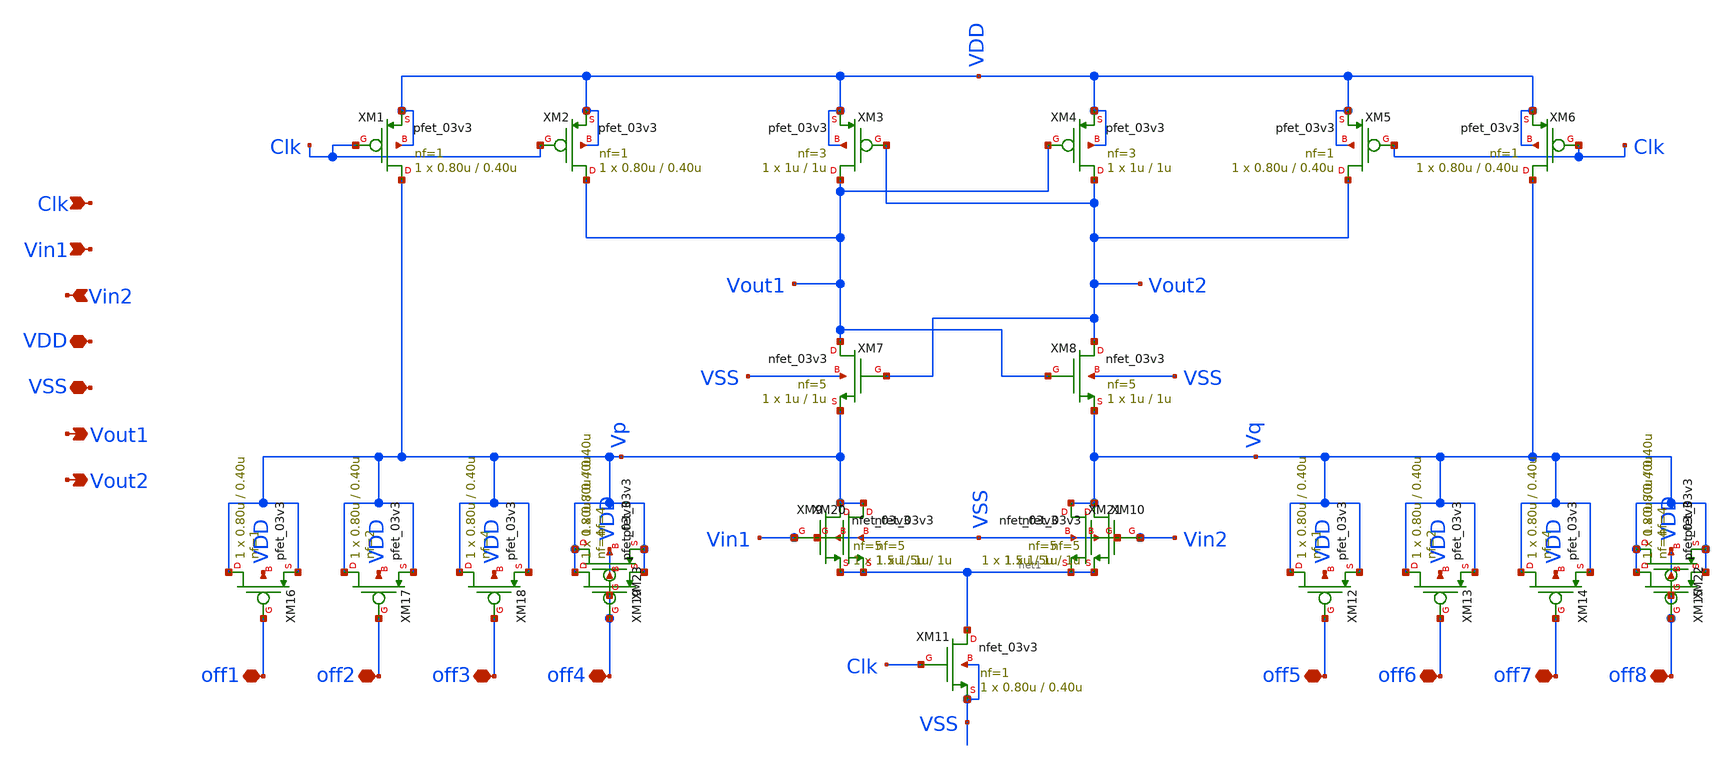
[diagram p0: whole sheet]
** sch_path: designs/comparator/final_magic/lvsclean_SAlatch.sch
**.subckt lvsclean_SAlatch Clk Vin1 Vin2 VDD VSS Vout1 Vout2 off5 off6 off7 off8 off1 off2 off3 off4
*.ipin Clk
*.ipin Vin1
*.ipin Vin2
*.iopin VDD
*.iopin VSS
*.opin Vout1
*.opin Vout2
*.iopin off5
*.iopin off6
*.iopin off7
*.iopin off8
*.iopin off1
*.iopin off2
*.iopin off3
*.iopin off4
XM1 Vp Clk VDD VDD pfet_03v3 L=0.40u W=0.80u nf=1 ad='int((nf+1)/2) * W/nf * 0.18u' as='int((nf+2)/2) * W/nf * 0.18u'
+ pd='2*int((nf+1)/2) * (W/nf + 0.18u)' ps='2*int((nf+2)/2) * (W/nf + 0.18u)' nrd='0.18u / W' nrs='0.18u / W'
+ sa=0 sb=0 sd=0 m=1
XM2 Vout1 Clk VDD VDD pfet_03v3 L=0.40u W=0.80u nf=1 ad='int((nf+1)/2) * W/nf * 0.18u' as='int((nf+2)/2) * W/nf * 0.18u'
+ pd='2*int((nf+1)/2) * (W/nf + 0.18u)' ps='2*int((nf+2)/2) * (W/nf + 0.18u)' nrd='0.18u / W' nrs='0.18u / W'
+ sa=0 sb=0 sd=0 m=1
XM3 Vout1 Vout2 VDD VDD pfet_03v3 L=1u W=1u nf=3 ad='int((nf+1)/2) * W/nf * 0.18u' as='int((nf+2)/2) * W/nf * 0.18u'
+ pd='2*int((nf+1)/2) * (W/nf + 0.18u)' ps='2*int((nf+2)/2) * (W/nf + 0.18u)' nrd='0.18u / W' nrs='0.18u / W'
+ sa=0 sb=0 sd=0 m=1
XM4 Vout2 Vout1 VDD VDD pfet_03v3 L=1u W=1u nf=3 ad='int((nf+1)/2) * W/nf * 0.18u' as='int((nf+2)/2) * W/nf * 0.18u'
+ pd='2*int((nf+1)/2) * (W/nf + 0.18u)' ps='2*int((nf+2)/2) * (W/nf + 0.18u)' nrd='0.18u / W' nrs='0.18u / W'
+ sa=0 sb=0 sd=0 m=1
XM5 Vout2 Clk VDD VDD pfet_03v3 L=0.40u W=0.80u nf=1 ad='int((nf+1)/2) * W/nf * 0.18u' as='int((nf+2)/2) * W/nf * 0.18u'
+ pd='2*int((nf+1)/2) * (W/nf + 0.18u)' ps='2*int((nf+2)/2) * (W/nf + 0.18u)' nrd='0.18u / W' nrs='0.18u / W'
+ sa=0 sb=0 sd=0 m=1
XM6 Vq Clk VDD VDD pfet_03v3 L=0.40u W=0.80u nf=1 ad='int((nf+1)/2) * W/nf * 0.18u' as='int((nf+2)/2) * W/nf * 0.18u'
+ pd='2*int((nf+1)/2) * (W/nf + 0.18u)' ps='2*int((nf+2)/2) * (W/nf + 0.18u)' nrd='0.18u / W' nrs='0.18u / W'
+ sa=0 sb=0 sd=0 m=1
XM7 Vout1 Vout2 Vp VSS nfet_03v3 L=1u W=1u nf=5 ad='int((nf+1)/2) * W/nf * 0.18u' as='int((nf+2)/2) * W/nf * 0.18u'
+ pd='2*int((nf+1)/2) * (W/nf + 0.18u)' ps='2*int((nf+2)/2) * (W/nf + 0.18u)' nrd='0.18u / W' nrs='0.18u / W'
+ sa=0 sb=0 sd=0 m=1
XM8 Vout2 Vout1 Vq VSS nfet_03v3 L=1u W=1u nf=5 ad='int((nf+1)/2) * W/nf * 0.18u' as='int((nf+2)/2) * W/nf * 0.18u'
+ pd='2*int((nf+1)/2) * (W/nf + 0.18u)' ps='2*int((nf+2)/2) * (W/nf + 0.18u)' nrd='0.18u / W' nrs='0.18u / W'
+ sa=0 sb=0 sd=0 m=1
XM9 Vp Vin1 net1 VSS nfet_03v3 L=1u W=1.5u nf=5 ad='int((nf+1)/2) * W/nf * 0.18u' as='int((nf+2)/2) * W/nf * 0.18u'
+ pd='2*int((nf+1)/2) * (W/nf + 0.18u)' ps='2*int((nf+2)/2) * (W/nf + 0.18u)' nrd='0.18u / W' nrs='0.18u / W'
+ sa=0 sb=0 sd=0 m=1
XM10 Vq Vin2 net1 VSS nfet_03v3 L=1u W=1.5u nf=5 ad='int((nf+1)/2) * W/nf * 0.18u' as='int((nf+2)/2) * W/nf * 0.18u'
+ pd='2*int((nf+1)/2) * (W/nf + 0.18u)' ps='2*int((nf+2)/2) * (W/nf + 0.18u)' nrd='0.18u / W' nrs='0.18u / W'
+ sa=0 sb=0 sd=0 m=1
XM11 net1 Clk VSS VSS nfet_03v3 L=0.40u W=0.80u nf=1 ad='int((nf+1)/2) * W/nf * 0.18u' as='int((nf+2)/2) * W/nf * 0.18u'
+ pd='2*int((nf+1)/2) * (W/nf + 0.18u)' ps='2*int((nf+2)/2) * (W/nf + 0.18u)' nrd='0.18u / W' nrs='0.18u / W'
+ sa=0 sb=0 sd=0 m=1
XM12 Vq off5 Vq VDD pfet_03v3 L=0.40u W=0.80u nf=1 ad='int((nf+1)/2) * W/nf * 0.18u' as='int((nf+2)/2) * W/nf * 0.18u'
+ pd='2*int((nf+1)/2) * (W/nf + 0.18u)' ps='2*int((nf+2)/2) * (W/nf + 0.18u)' nrd='0.18u / W' nrs='0.18u / W'
+ sa=0 sb=0 sd=0 m=1
XM13 Vq off6 Vq VDD pfet_03v3 L=0.40u W=0.80u nf=2 ad='int((nf+1)/2) * W/nf * 0.18u' as='int((nf+2)/2) * W/nf * 0.18u'
+ pd='2*int((nf+1)/2) * (W/nf + 0.18u)' ps='2*int((nf+2)/2) * (W/nf + 0.18u)' nrd='0.18u / W' nrs='0.18u / W'
+ sa=0 sb=0 sd=0 m=1
XM14 Vq off7 Vq VDD pfet_03v3 L=0.40u W=0.80u nf=4 ad='int((nf+1)/2) * W/nf * 0.18u' as='int((nf+2)/2) * W/nf * 0.18u'
+ pd='2*int((nf+1)/2) * (W/nf + 0.18u)' ps='2*int((nf+2)/2) * (W/nf + 0.18u)' nrd='0.18u / W' nrs='0.18u / W'
+ sa=0 sb=0 sd=0 m=1
XM15 Vq off8 Vq VDD pfet_03v3 L=0.40u W=0.80u nf=4 ad='int((nf+1)/2) * W/nf * 0.18u' as='int((nf+2)/2) * W/nf * 0.18u'
+ pd='2*int((nf+1)/2) * (W/nf + 0.18u)' ps='2*int((nf+2)/2) * (W/nf + 0.18u)' nrd='0.18u / W' nrs='0.18u / W'
+ sa=0 sb=0 sd=0 m=1
XM16 Vp off1 Vp VDD pfet_03v3 L=0.40u W=0.80u nf=1 ad='int((nf+1)/2) * W/nf * 0.18u' as='int((nf+2)/2) * W/nf * 0.18u'
+ pd='2*int((nf+1)/2) * (W/nf + 0.18u)' ps='2*int((nf+2)/2) * (W/nf + 0.18u)' nrd='0.18u / W' nrs='0.18u / W'
+ sa=0 sb=0 sd=0 m=1
XM17 Vp off2 Vp VDD pfet_03v3 L=0.40u W=0.80u nf=2 ad='int((nf+1)/2) * W/nf * 0.18u' as='int((nf+2)/2) * W/nf * 0.18u'
+ pd='2*int((nf+1)/2) * (W/nf + 0.18u)' ps='2*int((nf+2)/2) * (W/nf + 0.18u)' nrd='0.18u / W' nrs='0.18u / W'
+ sa=0 sb=0 sd=0 m=1
XM18 Vp off3 Vp VDD pfet_03v3 L=0.40u W=0.80u nf=4 ad='int((nf+1)/2) * W/nf * 0.18u' as='int((nf+2)/2) * W/nf * 0.18u'
+ pd='2*int((nf+1)/2) * (W/nf + 0.18u)' ps='2*int((nf+2)/2) * (W/nf + 0.18u)' nrd='0.18u / W' nrs='0.18u / W'
+ sa=0 sb=0 sd=0 m=1
XM19 Vp off4 Vp VDD pfet_03v3 L=0.40u W=0.80u nf=4 ad='int((nf+1)/2) * W/nf * 0.18u' as='int((nf+2)/2) * W/nf * 0.18u'
+ pd='2*int((nf+1)/2) * (W/nf + 0.18u)' ps='2*int((nf+2)/2) * (W/nf + 0.18u)' nrd='0.18u / W' nrs='0.18u / W'
+ sa=0 sb=0 sd=0 m=1
XM20 Vp Vin1 net1 VSS nfet_03v3 L=1u W=1.5u nf=5 ad='int((nf+1)/2) * W/nf * 0.18u' as='int((nf+2)/2) * W/nf * 0.18u'
+ pd='2*int((nf+1)/2) * (W/nf + 0.18u)' ps='2*int((nf+2)/2) * (W/nf + 0.18u)' nrd='0.18u / W' nrs='0.18u / W'
+ sa=0 sb=0 sd=0 m=1
XM21 Vq Vin2 net1 VSS nfet_03v3 L=1u W=1.5u nf=5 ad='int((nf+1)/2) * W/nf * 0.18u' as='int((nf+2)/2) * W/nf * 0.18u'
+ pd='2*int((nf+1)/2) * (W/nf + 0.18u)' ps='2*int((nf+2)/2) * (W/nf + 0.18u)' nrd='0.18u / W' nrs='0.18u / W'
+ sa=0 sb=0 sd=0 m=1
XM22 Vq off8 Vq VDD pfet_03v3 L=0.40u W=0.80u nf=4 ad='int((nf+1)/2) * W/nf * 0.18u' as='int((nf+2)/2) * W/nf * 0.18u'
+ pd='2*int((nf+1)/2) * (W/nf + 0.18u)' ps='2*int((nf+2)/2) * (W/nf + 0.18u)' nrd='0.18u / W' nrs='0.18u / W'
+ sa=0 sb=0 sd=0 m=1
XM23 Vp off4 Vp VDD pfet_03v3 L=0.40u W=0.80u nf=4 ad='int((nf+1)/2) * W/nf * 0.18u' as='int((nf+2)/2) * W/nf * 0.18u'
+ pd='2*int((nf+1)/2) * (W/nf + 0.18u)' ps='2*int((nf+2)/2) * (W/nf + 0.18u)' nrd='0.18u / W' nrs='0.18u / W'
+ sa=0 sb=0 sd=0 m=1
**.ends
.end
